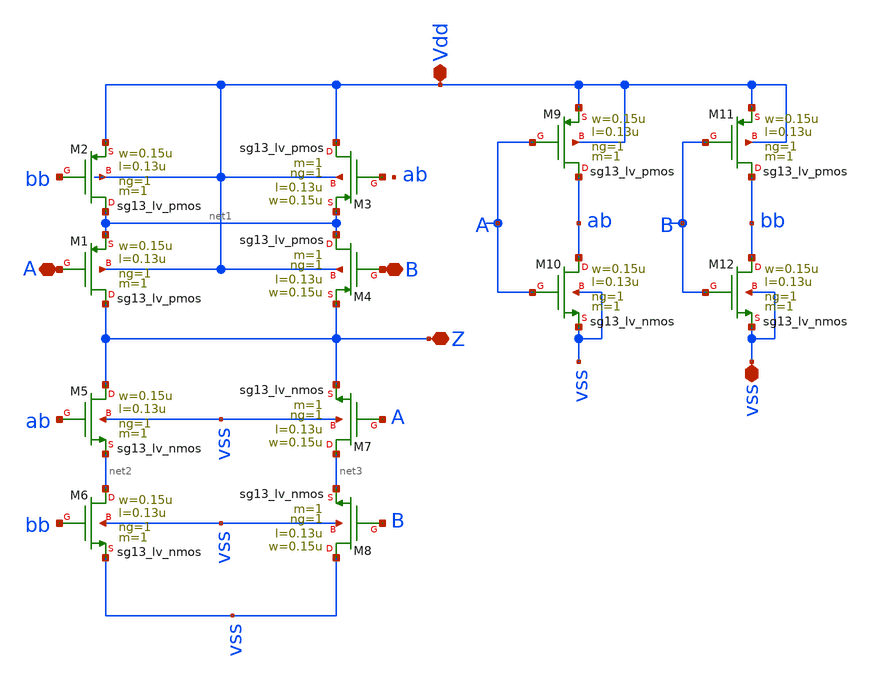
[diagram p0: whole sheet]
** sch_path: design/blocks/puertaxor/puertaxor.sch
**.subckt puertaxor A B vss Z Vdd
*.iopin A
*.iopin B
*.iopin vss
*.iopin Z
*.iopin Vdd
XM1 Z A net1 Vdd sg13_lv_pmos w=0.15u l=0.13u ng=1 m=1 mm_ok=1
XM2 net1 bb Vdd Vdd sg13_lv_pmos w=0.15u l=0.13u ng=1 m=1 mm_ok=1
XM3 Vdd net4 net1 Vdd sg13_lv_pmos w=0.15u l=0.13u ng=1 m=1 mm_ok=1
XM4 net1 B Z Vdd sg13_lv_pmos w=0.15u l=0.13u ng=1 m=1 mm_ok=1
XM5 Z ab net2 vss sg13_lv_nmos w=0.15u l=0.13u ng=1 m=1 mm_ok=1
XM6 net2 bb vss vss sg13_lv_nmos w=0.15u l=0.13u ng=1 m=1 mm_ok=1
XM7 net3 A Z vss sg13_lv_nmos w=0.15u l=0.13u ng=1 m=1 mm_ok=1
XM8 vss B net3 vss sg13_lv_nmos w=0.15u l=0.13u ng=1 m=1 mm_ok=1
XM9 ab A Vdd Vdd sg13_lv_pmos w=0.15u l=0.13u ng=1 m=1 mm_ok=1
XM10 ab A vss vss sg13_lv_nmos w=0.15u l=0.13u ng=1 m=1 mm_ok=1
XM11 bb B Vdd Vdd sg13_lv_pmos w=0.15u l=0.13u ng=1 m=1 mm_ok=1
XM12 bb B vss vss sg13_lv_nmos w=0.15u l=0.13u ng=1 m=1 mm_ok=1
**.ends
.end
